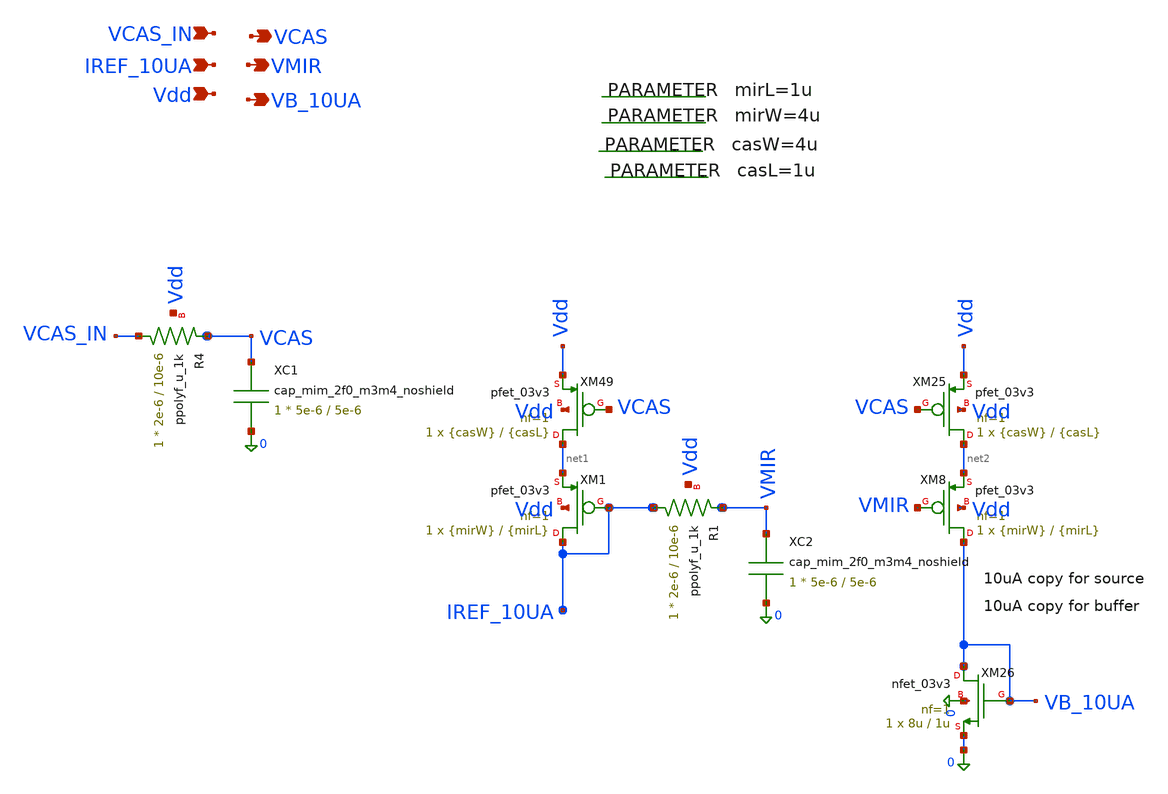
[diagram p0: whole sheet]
** sch_path: blocks/dac/cellv9/cell_iref.sch
**.subckt cell_iref VMIR VCAS Vdd VCAS_IN IREF_10UA VB_10UA
*.opin VMIR
*.opin VCAS
*.ipin Vdd
*.ipin VCAS_IN
*.ipin IREF_10UA
*.opin VB_10UA
XM1 IREF_10UA IREF_10UA net1 Vdd pfet_03v3 L={mirL} W={mirW} nf=1 ad='int((nf+1)/2) * W/nf * 0.18u' as='int((nf+2)/2) * W/nf * 0.18u'
+ pd='2*int((nf+1)/2) * (W/nf + 0.18u)' ps='2*int((nf+2)/2) * (W/nf + 0.18u)' nrd='0.18u / W' nrs='0.18u / W'
+ sa=0 sb=0 sd=0 m=1
XM49 net1 VCAS Vdd Vdd pfet_03v3 L={casL} W={casW} nf=1 ad='int((nf+1)/2) * W/nf * 0.18u' as='int((nf+2)/2) * W/nf * 0.18u'
+ pd='2*int((nf+1)/2) * (W/nf + 0.18u)' ps='2*int((nf+2)/2) * (W/nf + 0.18u)' nrd='0.18u / W' nrs='0.18u / W'
+ sa=0 sb=0 sd=0 m=1
XM8 VB_10UA VMIR net2 Vdd pfet_03v3 L={mirL} W={mirW} nf=1 ad='int((nf+1)/2) * W/nf * 0.18u' as='int((nf+2)/2) * W/nf * 0.18u'
+ pd='2*int((nf+1)/2) * (W/nf + 0.18u)' ps='2*int((nf+2)/2) * (W/nf + 0.18u)' nrd='0.18u / W' nrs='0.18u / W'
+ sa=0 sb=0 sd=0 m=1
XM25 net2 VCAS Vdd Vdd pfet_03v3 L={casL} W={casW} nf=1 ad='int((nf+1)/2) * W/nf * 0.18u' as='int((nf+2)/2) * W/nf * 0.18u'
+ pd='2*int((nf+1)/2) * (W/nf + 0.18u)' ps='2*int((nf+2)/2) * (W/nf + 0.18u)' nrd='0.18u / W' nrs='0.18u / W'
+ sa=0 sb=0 sd=0 m=1
XM26 VB_10UA VB_10UA 0 0 nfet_03v3 L=1u W=8u nf=1 ad='int((nf+1)/2) * W/nf * 0.18u' as='int((nf+2)/2) * W/nf * 0.18u'
+ pd='2*int((nf+1)/2) * (W/nf + 0.18u)' ps='2*int((nf+2)/2) * (W/nf + 0.18u)' nrd='0.18u / W' nrs='0.18u / W'
+ sa=0 sb=0 sd=0 m=1
XR4 VCAS_IN VCAS Vdd ppolyf_u_1k r_width=2e-6 r_length=10e-6 m=1
XC1 VCAS 0 cap_mim_2f0_m3m4_noshield c_width=5e-6 c_length=5e-6 m=1
.param casW=4u
.param mirW=4u
.param mirL=1u
.param casL=1u
XR1 IREF_10UA VMIR Vdd ppolyf_u_1k r_width=2e-6 r_length=10e-6 m=1
XC2 VMIR 0 cap_mim_2f0_m3m4_noshield c_width=5e-6 c_length=5e-6 m=1
**.ends
.end
